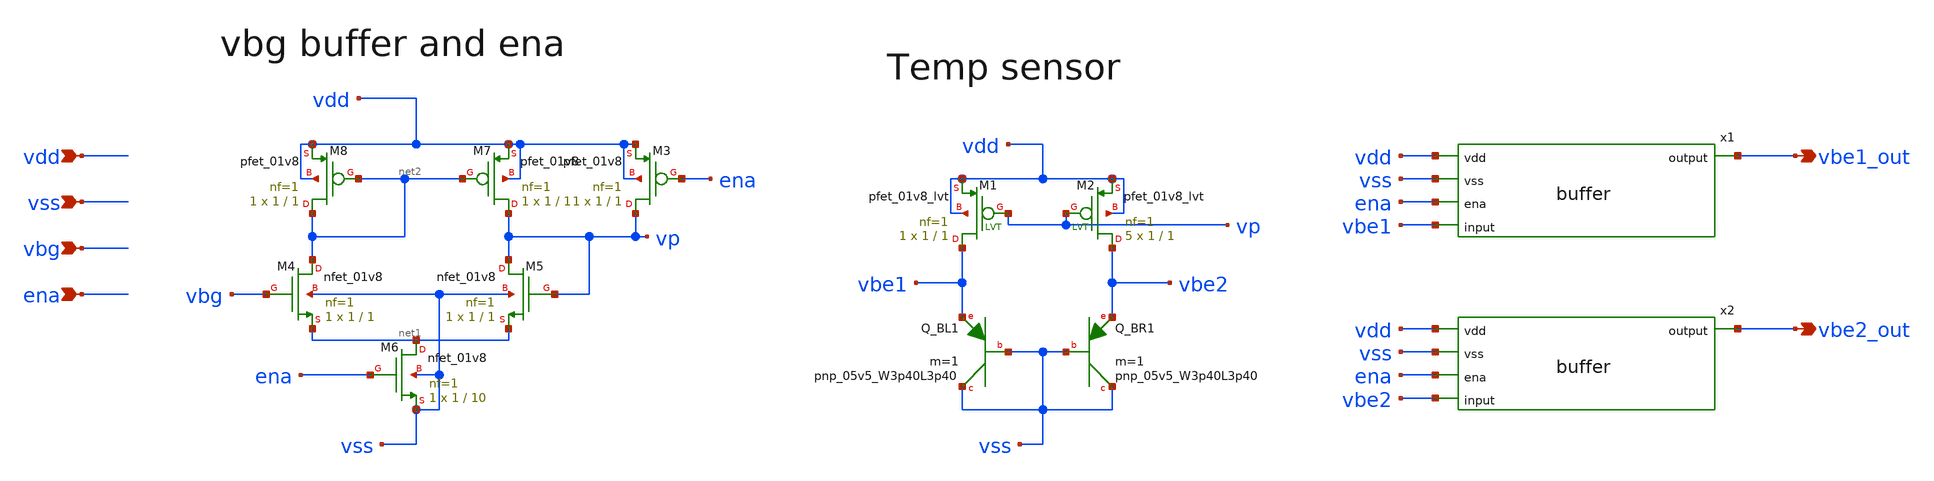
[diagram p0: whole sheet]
** sch_path: xschem/sky130_od_ip__tempsensor_ext_vp.sch
**.subckt sky130_od_ip__tempsensor_ext_vp vdd vss vbe2_out vbe1_out ena vbg
*.ipin vdd
*.ipin vss
*.opin vbe2_out
*.opin vbe1_out
*.ipin ena
*.ipin vbg
XQ_BL1 vss vss vbe1 sky130_fd_pr__pnp_05v5_W3p40L3p40 m=1
XQ_BR1 vss vss vbe2 sky130_fd_pr__pnp_05v5_W3p40L3p40 m=1
XM4 net2 vbg net1 vss sky130_fd_pr__nfet_01v8 L=1 W=1 nf=1 ad='int((nf+1)/2) * W/nf * 0.29' as='int((nf+2)/2) * W/nf * 0.29'
+ pd='2*int((nf+1)/2) * (W/nf + 0.29)' ps='2*int((nf+2)/2) * (W/nf + 0.29)' nrd='0.29 / W' nrs='0.29 / W'
+ sa=0 sb=0 sd=0 mult=1 m=1
XM5 vp vp net1 vss sky130_fd_pr__nfet_01v8 L=1 W=1 nf=1 ad='int((nf+1)/2) * W/nf * 0.29' as='int((nf+2)/2) * W/nf * 0.29'
+ pd='2*int((nf+1)/2) * (W/nf + 0.29)' ps='2*int((nf+2)/2) * (W/nf + 0.29)' nrd='0.29 / W' nrs='0.29 / W'
+ sa=0 sb=0 sd=0 mult=1 m=1
XM7 vp net2 vdd vdd sky130_fd_pr__pfet_01v8 L=1 W=1 nf=1 ad='int((nf+1)/2) * W/nf * 0.29' as='int((nf+2)/2) * W/nf * 0.29'
+ pd='2*int((nf+1)/2) * (W/nf + 0.29)' ps='2*int((nf+2)/2) * (W/nf + 0.29)' nrd='0.29 / W' nrs='0.29 / W'
+ sa=0 sb=0 sd=0 mult=1 m=1
XM8 net2 net2 vdd vdd sky130_fd_pr__pfet_01v8 L=1 W=1 nf=1 ad='int((nf+1)/2) * W/nf * 0.29' as='int((nf+2)/2) * W/nf * 0.29'
+ pd='2*int((nf+1)/2) * (W/nf + 0.29)' ps='2*int((nf+2)/2) * (W/nf + 0.29)' nrd='0.29 / W' nrs='0.29 / W'
+ sa=0 sb=0 sd=0 mult=1 m=1
XM3 vp ena vdd vdd sky130_fd_pr__pfet_01v8 L=1 W=1 nf=1 ad='int((nf+1)/2) * W/nf * 0.29' as='int((nf+2)/2) * W/nf * 0.29'
+ pd='2*int((nf+1)/2) * (W/nf + 0.29)' ps='2*int((nf+2)/2) * (W/nf + 0.29)' nrd='0.29 / W' nrs='0.29 / W'
+ sa=0 sb=0 sd=0 mult=1 m=1
XM6 net1 ena vss vss sky130_fd_pr__nfet_01v8 L=10 W=1 nf=1 ad='int((nf+1)/2) * W/nf * 0.29' as='int((nf+2)/2) * W/nf * 0.29'
+ pd='2*int((nf+1)/2) * (W/nf + 0.29)' ps='2*int((nf+2)/2) * (W/nf + 0.29)' nrd='0.29 / W' nrs='0.29 / W'
+ sa=0 sb=0 sd=0 mult=1 m=1
x1 vdd vss ena vbe1 vbe1_out buffer
x2 vdd vss ena vbe2 vbe2_out buffer
XM1 vbe1 vp vdd vdd sky130_fd_pr__pfet_01v8_lvt L=1 W=1 nf=1 ad='int((nf+1)/2) * W/nf * 0.29' as='int((nf+2)/2) * W/nf * 0.29'
+ pd='2*int((nf+1)/2) * (W/nf + 0.29)' ps='2*int((nf+2)/2) * (W/nf + 0.29)' nrd='0.29 / W' nrs='0.29 / W'
+ sa=0 sb=0 sd=0 mult=1 m=1
XM2 vbe2 vp vdd vdd sky130_fd_pr__pfet_01v8_lvt L=1 W=1 nf=1 ad='int((nf+1)/2) * W/nf * 0.29' as='int((nf+2)/2) * W/nf * 0.29'
+ pd='2*int((nf+1)/2) * (W/nf + 0.29)' ps='2*int((nf+2)/2) * (W/nf + 0.29)' nrd='0.29 / W' nrs='0.29 / W'
+ sa=0 sb=0 sd=0 mult=5 m=5
**.ends

* expanding   symbol:  xschem/buffer.sym # of pins=5
** sym_path: xschem/buffer.sym
** sch_path: xschem/buffer.sch
.subckt buffer vdd vss ena input output
*.opin output
*.ipin input
*.ipin vdd
*.ipin vss
*.ipin ena
XM1 net2 input net1 vss sky130_fd_pr__nfet_01v8 L=1 W=1 nf=1 ad='int((nf+1)/2) * W/nf * 0.29' as='int((nf+2)/2) * W/nf * 0.29'
+ pd='2*int((nf+1)/2) * (W/nf + 0.29)' ps='2*int((nf+2)/2) * (W/nf + 0.29)' nrd='0.29 / W' nrs='0.29 / W'
+ sa=0 sb=0 sd=0 mult=1 m=1
XM2 output output net1 vss sky130_fd_pr__nfet_01v8 L=1 W=1 nf=1 ad='int((nf+1)/2) * W/nf * 0.29' as='int((nf+2)/2) * W/nf * 0.29'
+ pd='2*int((nf+1)/2) * (W/nf + 0.29)' ps='2*int((nf+2)/2) * (W/nf + 0.29)' nrd='0.29 / W' nrs='0.29 / W'
+ sa=0 sb=0 sd=0 mult=1 m=1
XM5 net1 ena vss vss sky130_fd_pr__nfet_01v8 L=1 W=1 nf=1 ad='int((nf+1)/2) * W/nf * 0.29' as='int((nf+2)/2) * W/nf * 0.29'
+ pd='2*int((nf+1)/2) * (W/nf + 0.29)' ps='2*int((nf+2)/2) * (W/nf + 0.29)' nrd='0.29 / W' nrs='0.29 / W'
+ sa=0 sb=0 sd=0 mult=1 m=1
XM4 output net2 vdd vdd sky130_fd_pr__pfet_01v8 L=1 W=1 nf=1 ad='int((nf+1)/2) * W/nf * 0.29' as='int((nf+2)/2) * W/nf * 0.29'
+ pd='2*int((nf+1)/2) * (W/nf + 0.29)' ps='2*int((nf+2)/2) * (W/nf + 0.29)' nrd='0.29 / W' nrs='0.29 / W'
+ sa=0 sb=0 sd=0 mult=1 m=1
XM3 net2 net2 vdd vdd sky130_fd_pr__pfet_01v8 L=1 W=1 nf=1 ad='int((nf+1)/2) * W/nf * 0.29' as='int((nf+2)/2) * W/nf * 0.29'
+ pd='2*int((nf+1)/2) * (W/nf + 0.29)' ps='2*int((nf+2)/2) * (W/nf + 0.29)' nrd='0.29 / W' nrs='0.29 / W'
+ sa=0 sb=0 sd=0 mult=1 m=1
.ends

.end
